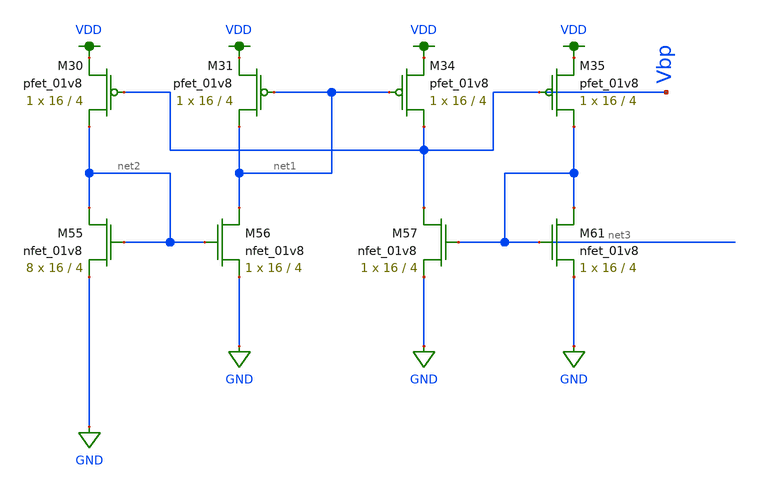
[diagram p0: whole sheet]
** sch_path: schematic/LDS/test/ibias_vgt_oglvs.sch
**.subckt ibias_vgt_oglvs
XM30 net2 Vbp VDD VDD sky130_fd_pr__pfet_01v8 L=4 W=16 nf=1 ad='int((nf+1)/2) * W/nf * 0.29' as='int((nf+2)/2) * W/nf * 0.29'
+ pd='2*int((nf+1)/2) * (W/nf + 0.29)' ps='2*int((nf+2)/2) * (W/nf + 0.29)' nrd='0.29 / W' nrs='0.29 / W'
+ sa=0 sb=0 sd=0 mult=1 m=1
XM31 net1 net1 VDD VDD sky130_fd_pr__pfet_01v8 L=4 W=16 nf=1 ad='int((nf+1)/2) * W/nf * 0.29' as='int((nf+2)/2) * W/nf * 0.29'
+ pd='2*int((nf+1)/2) * (W/nf + 0.29)' ps='2*int((nf+2)/2) * (W/nf + 0.29)' nrd='0.29 / W' nrs='0.29 / W'
+ sa=0 sb=0 sd=0 mult=1 m=1
XM34 Vbp net1 VDD VDD sky130_fd_pr__pfet_01v8 L=4 W=16 nf=1 ad='int((nf+1)/2) * W/nf * 0.29' as='int((nf+2)/2) * W/nf * 0.29'
+ pd='2*int((nf+1)/2) * (W/nf + 0.29)' ps='2*int((nf+2)/2) * (W/nf + 0.29)' nrd='0.29 / W' nrs='0.29 / W'
+ sa=0 sb=0 sd=0 mult=1 m=1
XM35 net3 Vbp VDD VDD sky130_fd_pr__pfet_01v8 L=4 W=16 nf=1 ad='int((nf+1)/2) * W/nf * 0.29' as='int((nf+2)/2) * W/nf * 0.29'
+ pd='2*int((nf+1)/2) * (W/nf + 0.29)' ps='2*int((nf+2)/2) * (W/nf + 0.29)' nrd='0.29 / W' nrs='0.29 / W'
+ sa=0 sb=0 sd=0 mult=1 m=1
XM55 net2 net2 GND GND sky130_fd_pr__nfet_01v8 L=4 W=16 nf=1 ad='int((nf+1)/2) * W/nf * 0.29' as='int((nf+2)/2) * W/nf * 0.29'
+ pd='2*int((nf+1)/2) * (W/nf + 0.29)' ps='2*int((nf+2)/2) * (W/nf + 0.29)' nrd='0.29 / W' nrs='0.29 / W'
+ sa=0 sb=0 sd=0 mult=8 m=8
XM56 net1 net2 GND GND sky130_fd_pr__nfet_01v8 L=4 W=16 nf=1 ad='int((nf+1)/2) * W/nf * 0.29' as='int((nf+2)/2) * W/nf * 0.29'
+ pd='2*int((nf+1)/2) * (W/nf + 0.29)' ps='2*int((nf+2)/2) * (W/nf + 0.29)' nrd='0.29 / W' nrs='0.29 / W'
+ sa=0 sb=0 sd=0 mult=1 m=1
XM57 Vbp net3 GND GND sky130_fd_pr__nfet_01v8 L=4 W=16 nf=1 ad='int((nf+1)/2) * W/nf * 0.29' as='int((nf+2)/2) * W/nf * 0.29'
+ pd='2*int((nf+1)/2) * (W/nf + 0.29)' ps='2*int((nf+2)/2) * (W/nf + 0.29)' nrd='0.29 / W' nrs='0.29 / W'
+ sa=0 sb=0 sd=0 mult=1 m=1
XM61 net3 net3 GND GND sky130_fd_pr__nfet_01v8 L=4 W=16 nf=1 ad='int((nf+1)/2) * W/nf * 0.29' as='int((nf+2)/2) * W/nf * 0.29'
+ pd='2*int((nf+1)/2) * (W/nf + 0.29)' ps='2*int((nf+2)/2) * (W/nf + 0.29)' nrd='0.29 / W' nrs='0.29 / W'
+ sa=0 sb=0 sd=0 mult=1 m=1
**.ends
.GLOBAL GND
.GLOBAL VDD
.end
